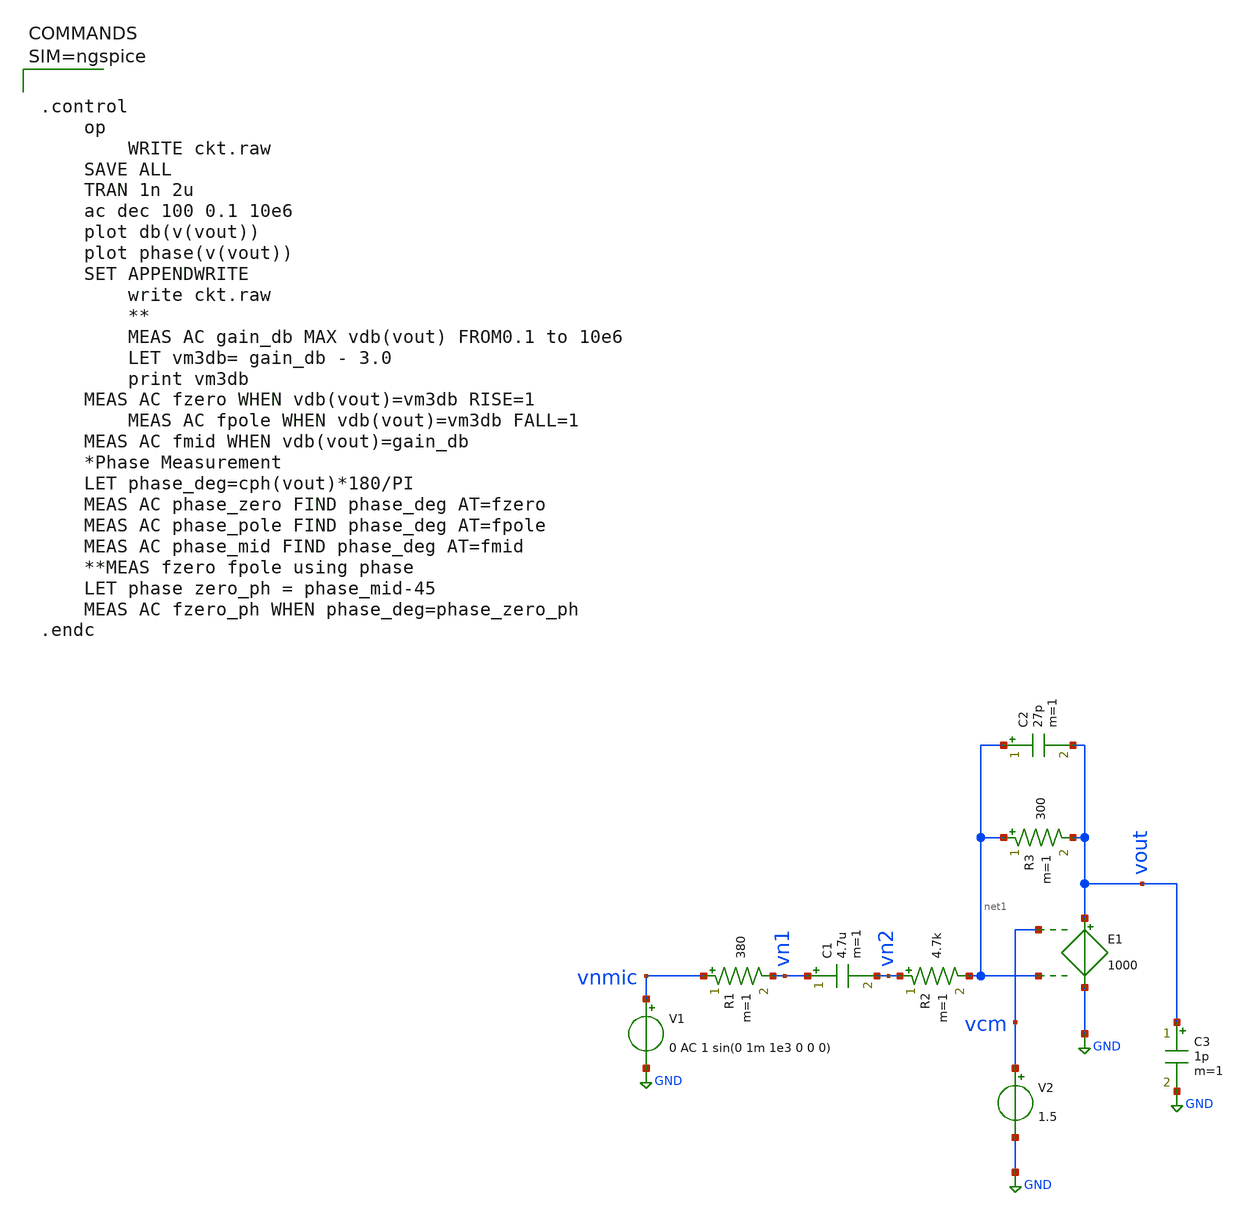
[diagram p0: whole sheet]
** sch_path: xschem/micTest.sch
**.subckt micTest
V1 vnmic GND 0 AC 1 sin(0 1m 1e3 0 0 0)
C1 vn1 vn2 4.7u m=1
R1 vnmic vn1 380 m=1
R2 vn2 net1 4.7k m=1
E1 vout GND vcm net1 1000
R3 net1 vout 300 m=1
C2 net1 vout 27p m=1
C3 vout GND 1p m=1
V2 vcm GND 1.5
**** begin user architecture code



.control
	op
        WRITE ckt.raw
	SAVE ALL
	TRAN 1n 2u
	ac dec 100 0.1 10e6
	plot db(v(vout))
	plot phase(v(vout))
	SET APPENDWRITE
        write ckt.raw
        **
        MEAS AC gain_db MAX vdb(vout) FROM0.1 to 10e6
        LET vm3db= gain_db - 3.0
        print vm3db
	MEAS AC fzero WHEN vdb(vout)=vm3db RISE=1
        MEAS AC fpole WHEN vdb(vout)=vm3db FALL=1
	MEAS AC fmid WHEN vdb(vout)=gain_db
	*Phase Measurement
	LET phase_deg=cph(vout)*180/PI
	MEAS AC phase_zero FIND phase_deg AT=fzero
	MEAS AC phase_pole FIND phase_deg AT=fpole
	MEAS AC phase_mid FIND phase_deg AT=fmid
	**MEAS fzero fpole using phase
	LET phase zero_ph = phase_mid-45
	MEAS AC fzero_ph WHEN phase_deg=phase_zero_ph
.endc



**** end user architecture code
**.ends
.GLOBAL GND
.end
